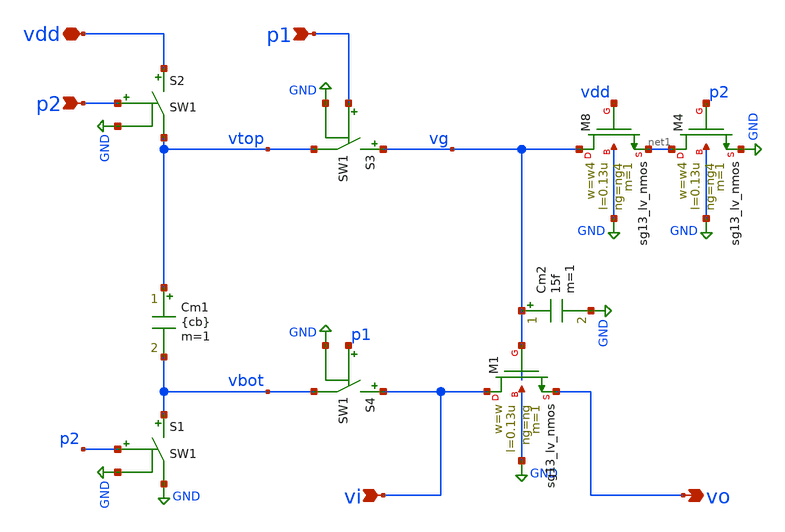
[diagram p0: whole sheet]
** sch_path: xschem/boot2.sch
**.subckt boot2 vi vo p2 p1 vdd
*.ipin vi
*.opin vo
*.ipin p2
*.ipin p1
*.iopin vdd
Cm1 vtop vbot {cb} m=1
S1 vbot GND p2 GND SW1
S2 vdd vtop p2 GND SW1
S3 vg vtop p1 GND SW1
S4 vi vbot p1 GND SW1
XM1 vi vg vo GND sg13_lv_nmos w=w l=0.13u ng=ng m=1 mm_ok=1
XM8 vg vdd net1 GND sg13_lv_nmos w=w4 l=0.13u ng=ng4 m=1 mm_ok=1
XM4 net1 p2 GND GND sg13_lv_nmos w=w4 l=0.13u ng=ng4 m=1 mm_ok=1
Cm2 vg GND 15f m=1
**.ends
.GLOBAL GND
**** begin user architecture code
.MODEL SW1 SW   VT=0.6 VH=vh  RON=rsw ROFF=roff
**** end user architecture code
.end
